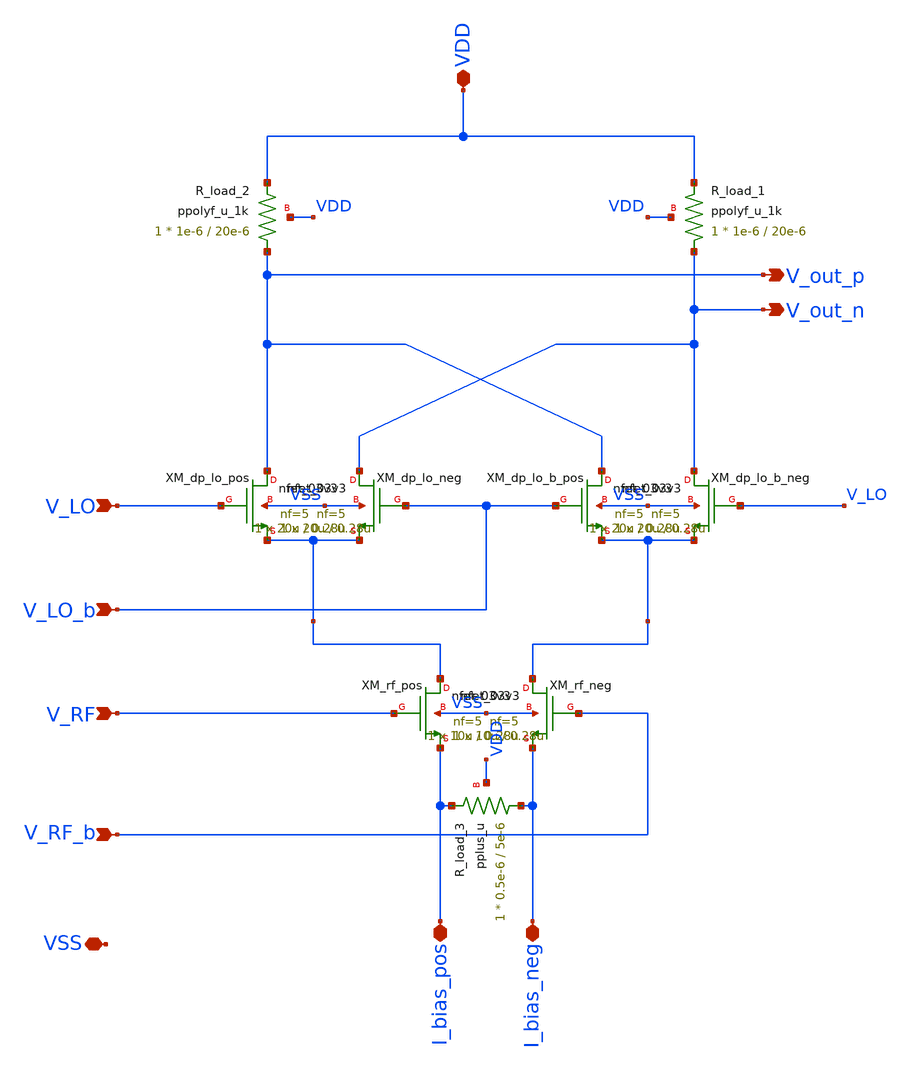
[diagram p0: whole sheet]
** sch_path: src/design_xsch/experimental_hierarchal/Gilbert_cell_no_hierarchy.sch
**.subckt Gilbert_cell_no_hierarchy V_LO V_LO_b V_RF V_RF_b V_out_p V_out_n I_bias_neg I_bias_pos
*+ VDD VSS
*.ipin V_LO
*.ipin V_LO_b
*.ipin V_RF
*.ipin V_RF_b
*.opin V_out_p
*.opin V_out_n
*.iopin I_bias_neg
*.iopin I_bias_pos
*.iopin VDD
*.iopin VSS
XM_dp_lo_pos V_out_p V_LO rf_diff_pair_pos_input VSS nfet_03v3 L=0.28u W=20u nf=5 ad='int((nf+1)/2) * W/nf * 0.18u'
+ as='int((nf+2)/2) * W/nf * 0.18u' pd='2*int((nf+1)/2) * (W/nf + 0.18u)' ps='2*int((nf+2)/2) * (W/nf + 0.18u)'
+ nrd='0.18u / W' nrs='0.18u / W' sa=0 sb=0 sd=0 m=1
XM_dp_lo_neg V_out_n V_LO_b rf_diff_pair_pos_input VSS nfet_03v3 L=0.28u W=20u nf=5 ad='int((nf+1)/2) * W/nf * 0.18u'
+ as='int((nf+2)/2) * W/nf * 0.18u' pd='2*int((nf+1)/2) * (W/nf + 0.18u)' ps='2*int((nf+2)/2) * (W/nf + 0.18u)'
+ nrd='0.18u / W' nrs='0.18u / W' sa=0 sb=0 sd=0 m=1
XM_dp_lo_b_pos V_out_p V_LO_b rf_diff_pair_neg_input VSS nfet_03v3 L=0.28u W=20u nf=5 ad='int((nf+1)/2) * W/nf * 0.18u'
+ as='int((nf+2)/2) * W/nf * 0.18u' pd='2*int((nf+1)/2) * (W/nf + 0.18u)' ps='2*int((nf+2)/2) * (W/nf + 0.18u)'
+ nrd='0.18u / W' nrs='0.18u / W' sa=0 sb=0 sd=0 m=1
XM_dp_lo_b_neg V_out_n V_LO rf_diff_pair_neg_input VSS nfet_03v3 L=0.28u W=20u nf=5 ad='int((nf+1)/2) * W/nf * 0.18u'
+ as='int((nf+2)/2) * W/nf * 0.18u' pd='2*int((nf+1)/2) * (W/nf + 0.18u)' ps='2*int((nf+2)/2) * (W/nf + 0.18u)'
+ nrd='0.18u / W' nrs='0.18u / W' sa=0 sb=0 sd=0 m=1
XM_rf_pos rf_diff_pair_pos_input V_RF I_bias_pos VSS nfet_03v3 L=0.28u W=10u nf=5 ad='int((nf+1)/2) * W/nf * 0.18u'
+ as='int((nf+2)/2) * W/nf * 0.18u' pd='2*int((nf+1)/2) * (W/nf + 0.18u)' ps='2*int((nf+2)/2) * (W/nf + 0.18u)'
+ nrd='0.18u / W' nrs='0.18u / W' sa=0 sb=0 sd=0 m=1
XM_rf_neg rf_diff_pair_neg_input V_RF_b I_bias_neg VSS nfet_03v3 L=0.28u W=10u nf=5 ad='int((nf+1)/2) * W/nf * 0.18u'
+ as='int((nf+2)/2) * W/nf * 0.18u' pd='2*int((nf+1)/2) * (W/nf + 0.18u)' ps='2*int((nf+2)/2) * (W/nf + 0.18u)'
+ nrd='0.18u / W' nrs='0.18u / W' sa=0 sb=0 sd=0 m=1
XR_load_3 I_bias_neg I_bias_pos VDD pplus_u r_width=0.5e-6 r_length=5e-6 m=1
XR_load_2 V_out_p VDD VDD ppolyf_u_1k r_width=1e-6 r_length=20e-6 m=1
XR_load_1 V_out_n VDD VDD ppolyf_u_1k r_width=1e-6 r_length=20e-6 m=1
**.ends
.end
